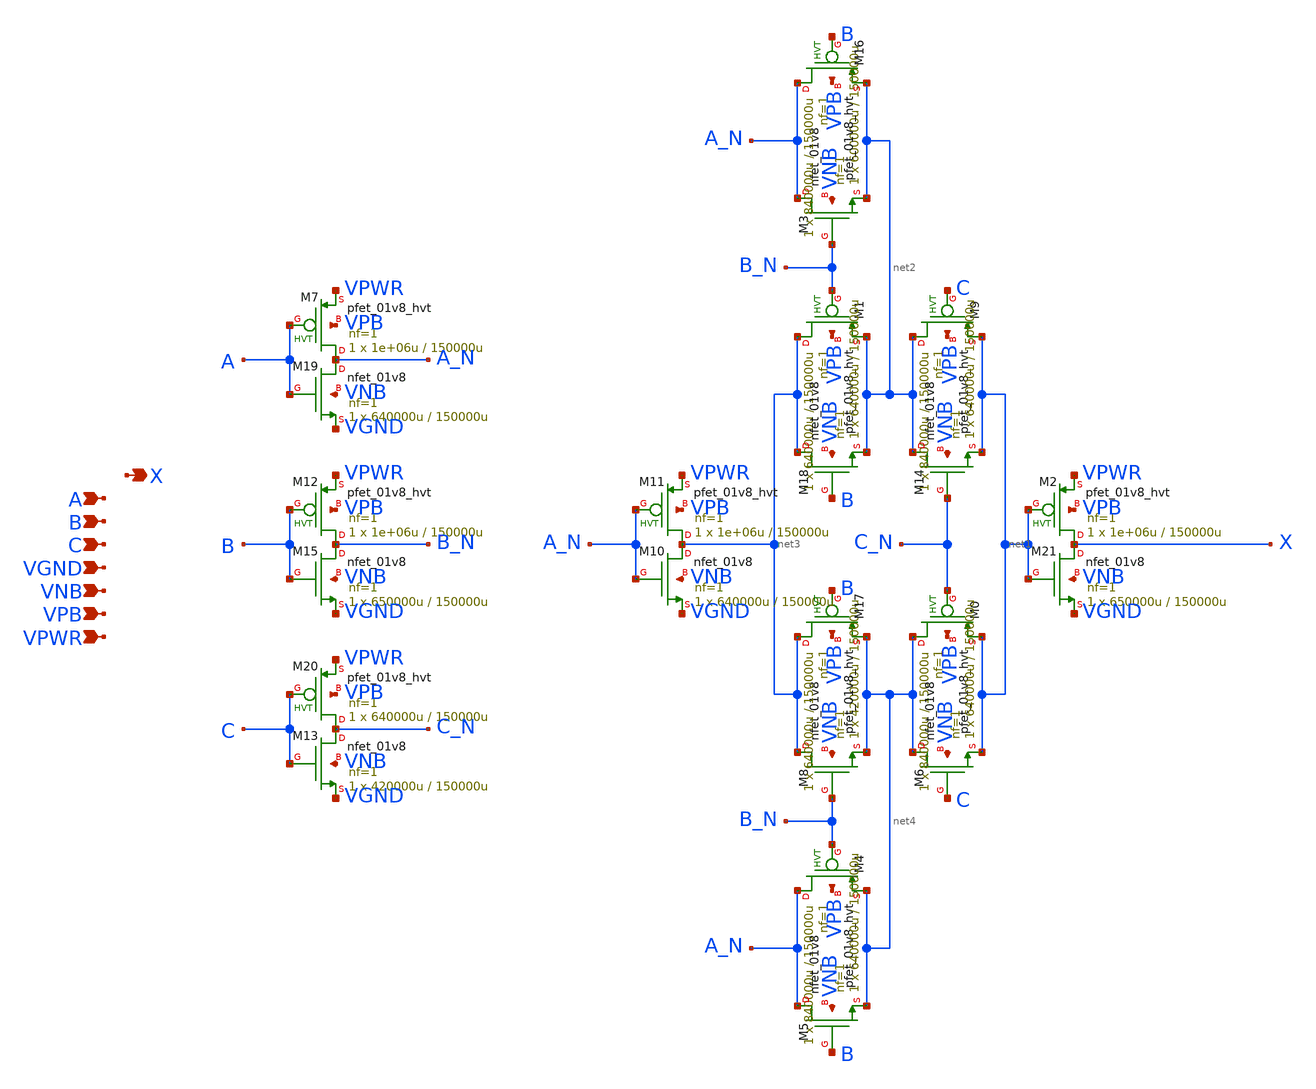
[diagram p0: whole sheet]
** sch_path: schematics/xor3/sky130_fd_sc_hd__xor3_1.sch
**.subckt sky130_fd_sc_hd__xor3_1 A B C VGND VNB VPB VPWR X
*.ipin A
*.ipin B
*.ipin C
*.ipin VGND
*.ipin VNB
*.ipin VPB
*.ipin VPWR
*.opin X
XM0 net4 C_N net1 VPB sky130_fd_pr__pfet_01v8_hvt L=150000u W=840000u nf=1 ad='int((1 + 1)/2) * 840000u / 1 * 0.29'
+ as='int((1 + 2)/2) * 840000u / 1 * 0.29' pd='2*int((1 + 1)/2) * (840000u / 1 + 0.29)' ps='2*int((1 + 2)/2) * (840000u / 1 + 0.29)'
+ nrd='0.29 / 840000u ' nrs='0.29 / 840000u ' sa=0 sb=0 sd=0 mult=1 m=1
XM1 net3 B_N net2 VPB sky130_fd_pr__pfet_01v8_hvt L=150000u W=640000u nf=1 ad='int((1 + 1)/2) * 640000u / 1 * 0.29'
+ as='int((1 + 2)/2) * 640000u / 1 * 0.29' pd='2*int((1 + 1)/2) * (640000u / 1 + 0.29)' ps='2*int((1 + 2)/2) * (640000u / 1 + 0.29)'
+ nrd='0.29 / 640000u ' nrs='0.29 / 640000u ' sa=0 sb=0 sd=0 mult=1 m=1
XM2 X net1 VPWR VPB sky130_fd_pr__pfet_01v8_hvt L=150000u W=1e+06u nf=1 ad='int((1 + 1)/2) * 1e+06u / 1 * 0.29'
+ as='int((1 + 2)/2) * 1e+06u / 1 * 0.29' pd='2*int((1 + 1)/2) * (1e+06u / 1 + 0.29)' ps='2*int((1 + 2)/2) * (1e+06u / 1 + 0.29)'
+ nrd='0.29 / 1e+06u ' nrs='0.29 / 1e+06u ' sa=0 sb=0 sd=0 mult=1 m=1
XM3 A_N B_N net2 VNB sky130_fd_pr__nfet_01v8 L=150000u W=600000u nf=1 ad='int((1 + 1)/2) * 600000u / 1 * 0.29'
+ as='int((1 + 2)/2) * 600000u / 1 * 0.29' pd='2*int((1 + 1)/2) * (600000u / 1 + 0.29)' ps='2*int((1 + 2)/2) * (600000u / 1 + 0.29)'
+ nrd='0.29 / 600000u ' nrs='0.29 / 600000u ' sa=0 sb=0 sd=0 mult=1 m=1
XM4 A_N B_N net4 VPB sky130_fd_pr__pfet_01v8_hvt L=150000u W=840000u nf=1 ad='int((1 + 1)/2) * 840000u / 1 * 0.29'
+ as='int((1 + 2)/2) * 840000u / 1 * 0.29' pd='2*int((1 + 1)/2) * (840000u / 1 + 0.29)' ps='2*int((1 + 2)/2) * (840000u / 1 + 0.29)'
+ nrd='0.29 / 840000u ' nrs='0.29 / 840000u ' sa=0 sb=0 sd=0 mult=1 m=1
XM5 A_N B net4 VNB sky130_fd_pr__nfet_01v8 L=150000u W=640000u nf=1 ad='int((1 + 1)/2) * 640000u / 1 * 0.29'
+ as='int((1 + 2)/2) * 640000u / 1 * 0.29' pd='2*int((1 + 1)/2) * (640000u / 1 + 0.29)' ps='2*int((1 + 2)/2) * (640000u / 1 + 0.29)'
+ nrd='0.29 / 640000u ' nrs='0.29 / 640000u ' sa=0 sb=0 sd=0 mult=1 m=1
XM6 net4 C net1 VNB sky130_fd_pr__nfet_01v8 L=150000u W=640000u nf=1 ad='int((1 + 1)/2) * 640000u / 1 * 0.29'
+ as='int((1 + 2)/2) * 640000u / 1 * 0.29' pd='2*int((1 + 1)/2) * (640000u / 1 + 0.29)' ps='2*int((1 + 2)/2) * (640000u / 1 + 0.29)'
+ nrd='0.29 / 640000u ' nrs='0.29 / 640000u ' sa=0 sb=0 sd=0 mult=1 m=1
XM7 A_N A VPWR VPB sky130_fd_pr__pfet_01v8_hvt L=150000u W=1e+06u nf=1 ad='int((1 + 1)/2) * 1e+06u / 1 * 0.29'
+ as='int((1 + 2)/2) * 1e+06u / 1 * 0.29' pd='2*int((1 + 1)/2) * (1e+06u / 1 + 0.29)' ps='2*int((1 + 2)/2) * (1e+06u / 1 + 0.29)'
+ nrd='0.29 / 1e+06u ' nrs='0.29 / 1e+06u ' sa=0 sb=0 sd=0 mult=1 m=1
XM8 net3 B_N net4 VNB sky130_fd_pr__nfet_01v8 L=150000u W=420000u nf=1 ad='int((1 + 1)/2) * 420000u / 1 * 0.29'
+ as='int((1 + 2)/2) * 420000u / 1 * 0.29' pd='2*int((1 + 1)/2) * (420000u / 1 + 0.29)' ps='2*int((1 + 2)/2) * (420000u / 1 + 0.29)'
+ nrd='0.29 / 420000u ' nrs='0.29 / 420000u ' sa=0 sb=0 sd=0 mult=1 m=1
XM9 net2 C net1 VPB sky130_fd_pr__pfet_01v8_hvt L=150000u W=840000u nf=1 ad='int((1 + 1)/2) * 840000u / 1 * 0.29'
+ as='int((1 + 2)/2) * 840000u / 1 * 0.29' pd='2*int((1 + 1)/2) * (840000u / 1 + 0.29)' ps='2*int((1 + 2)/2) * (840000u / 1 + 0.29)'
+ nrd='0.29 / 840000u ' nrs='0.29 / 840000u ' sa=0 sb=0 sd=0 mult=1 m=1
XM10 net3 A_N VGND VNB sky130_fd_pr__nfet_01v8 L=150000u W=640000u nf=1 ad='int((1 + 1)/2) * 640000u / 1 * 0.29'
+ as='int((1 + 2)/2) * 640000u / 1 * 0.29' pd='2*int((1 + 1)/2) * (640000u / 1 + 0.29)' ps='2*int((1 + 2)/2) * (640000u / 1 + 0.29)'
+ nrd='0.29 / 640000u ' nrs='0.29 / 640000u ' sa=0 sb=0 sd=0 mult=1 m=1
XM11 net3 A_N VPWR VPB sky130_fd_pr__pfet_01v8_hvt L=150000u W=1e+06u nf=1 ad='int((1 + 1)/2) * 1e+06u / 1 * 0.29'
+ as='int((1 + 2)/2) * 1e+06u / 1 * 0.29' pd='2*int((1 + 1)/2) * (1e+06u / 1 + 0.29)' ps='2*int((1 + 2)/2) * (1e+06u / 1 + 0.29)'
+ nrd='0.29 / 1e+06u ' nrs='0.29 / 1e+06u ' sa=0 sb=0 sd=0 mult=1 m=1
XM12 B_N B VPWR VPB sky130_fd_pr__pfet_01v8_hvt L=150000u W=1e+06u nf=1 ad='int((1 + 1)/2) * 1e+06u / 1 * 0.29'
+ as='int((1 + 2)/2) * 1e+06u / 1 * 0.29' pd='2*int((1 + 1)/2) * (1e+06u / 1 + 0.29)' ps='2*int((1 + 2)/2) * (1e+06u / 1 + 0.29)'
+ nrd='0.29 / 1e+06u ' nrs='0.29 / 1e+06u ' sa=0 sb=0 sd=0 mult=1 m=1
XM13 C_N C VGND VNB sky130_fd_pr__nfet_01v8 L=150000u W=420000u nf=1 ad='int((1 + 1)/2) * 420000u / 1 * 0.29'
+ as='int((1 + 2)/2) * 420000u / 1 * 0.29' pd='2*int((1 + 1)/2) * (420000u / 1 + 0.29)' ps='2*int((1 + 2)/2) * (420000u / 1 + 0.29)'
+ nrd='0.29 / 420000u ' nrs='0.29 / 420000u ' sa=0 sb=0 sd=0 mult=1 m=1
XM14 net2 C_N net1 VNB sky130_fd_pr__nfet_01v8 L=150000u W=640000u nf=1 ad='int((1 + 1)/2) * 640000u / 1 * 0.29'
+ as='int((1 + 2)/2) * 640000u / 1 * 0.29' pd='2*int((1 + 1)/2) * (640000u / 1 + 0.29)' ps='2*int((1 + 2)/2) * (640000u / 1 + 0.29)'
+ nrd='0.29 / 640000u ' nrs='0.29 / 640000u ' sa=0 sb=0 sd=0 mult=1 m=1
XM15 B_N B VGND VNB sky130_fd_pr__nfet_01v8 L=150000u W=650000u nf=1 ad='int((1 + 1)/2) * 650000u / 1 * 0.29'
+ as='int((1 + 2)/2) * 650000u / 1 * 0.29' pd='2*int((1 + 1)/2) * (650000u / 1 + 0.29)' ps='2*int((1 + 2)/2) * (650000u / 1 + 0.29)'
+ nrd='0.29 / 650000u ' nrs='0.29 / 650000u ' sa=0 sb=0 sd=0 mult=1 m=1
XM16 A_N B net2 VPB sky130_fd_pr__pfet_01v8_hvt L=150000u W=840000u nf=1 ad='int((1 + 1)/2) * 840000u / 1 * 0.29'
+ as='int((1 + 2)/2) * 840000u / 1 * 0.29' pd='2*int((1 + 1)/2) * (840000u / 1 + 0.29)' ps='2*int((1 + 2)/2) * (840000u / 1 + 0.29)'
+ nrd='0.29 / 840000u ' nrs='0.29 / 840000u ' sa=0 sb=0 sd=0 mult=1 m=1
XM17 net3 B net4 VPB sky130_fd_pr__pfet_01v8_hvt L=150000u W=640000u nf=1 ad='int((1 + 1)/2) * 640000u / 1 * 0.29'
+ as='int((1 + 2)/2) * 640000u / 1 * 0.29' pd='2*int((1 + 1)/2) * (640000u / 1 + 0.29)' ps='2*int((1 + 2)/2) * (640000u / 1 + 0.29)'
+ nrd='0.29 / 640000u ' nrs='0.29 / 640000u ' sa=0 sb=0 sd=0 mult=1 m=1
XM18 net3 B net2 VNB sky130_fd_pr__nfet_01v8 L=150000u W=640000u nf=1 ad='int((1 + 1)/2) * 640000u / 1 * 0.29'
+ as='int((1 + 2)/2) * 640000u / 1 * 0.29' pd='2*int((1 + 1)/2) * (640000u / 1 + 0.29)' ps='2*int((1 + 2)/2) * (640000u / 1 + 0.29)'
+ nrd='0.29 / 640000u ' nrs='0.29 / 640000u ' sa=0 sb=0 sd=0 mult=1 m=1
XM19 A_N A VGND VNB sky130_fd_pr__nfet_01v8 L=150000u W=640000u nf=1 ad='int((1 + 1)/2) * 640000u / 1 * 0.29'
+ as='int((1 + 2)/2) * 640000u / 1 * 0.29' pd='2*int((1 + 1)/2) * (640000u / 1 + 0.29)' ps='2*int((1 + 2)/2) * (640000u / 1 + 0.29)'
+ nrd='0.29 / 640000u ' nrs='0.29 / 640000u ' sa=0 sb=0 sd=0 mult=1 m=1
XM20 C_N C VPWR VPB sky130_fd_pr__pfet_01v8_hvt L=150000u W=640000u nf=1 ad='int((1 + 1)/2) * 640000u / 1 * 0.29'
+ as='int((1 + 2)/2) * 640000u / 1 * 0.29' pd='2*int((1 + 1)/2) * (640000u / 1 + 0.29)' ps='2*int((1 + 2)/2) * (640000u / 1 + 0.29)'
+ nrd='0.29 / 640000u ' nrs='0.29 / 640000u ' sa=0 sb=0 sd=0 mult=1 m=1
XM21 X net1 VGND VNB sky130_fd_pr__nfet_01v8 L=150000u W=650000u nf=1 ad='int((1 + 1)/2) * 650000u / 1 * 0.29'
+ as='int((1 + 2)/2) * 650000u / 1 * 0.29' pd='2*int((1 + 1)/2) * (650000u / 1 + 0.29)' ps='2*int((1 + 2)/2) * (650000u / 1 + 0.29)'
+ nrd='0.29 / 650000u ' nrs='0.29 / 650000u ' sa=0 sb=0 sd=0 mult=1 m=1
**.ends
.end
